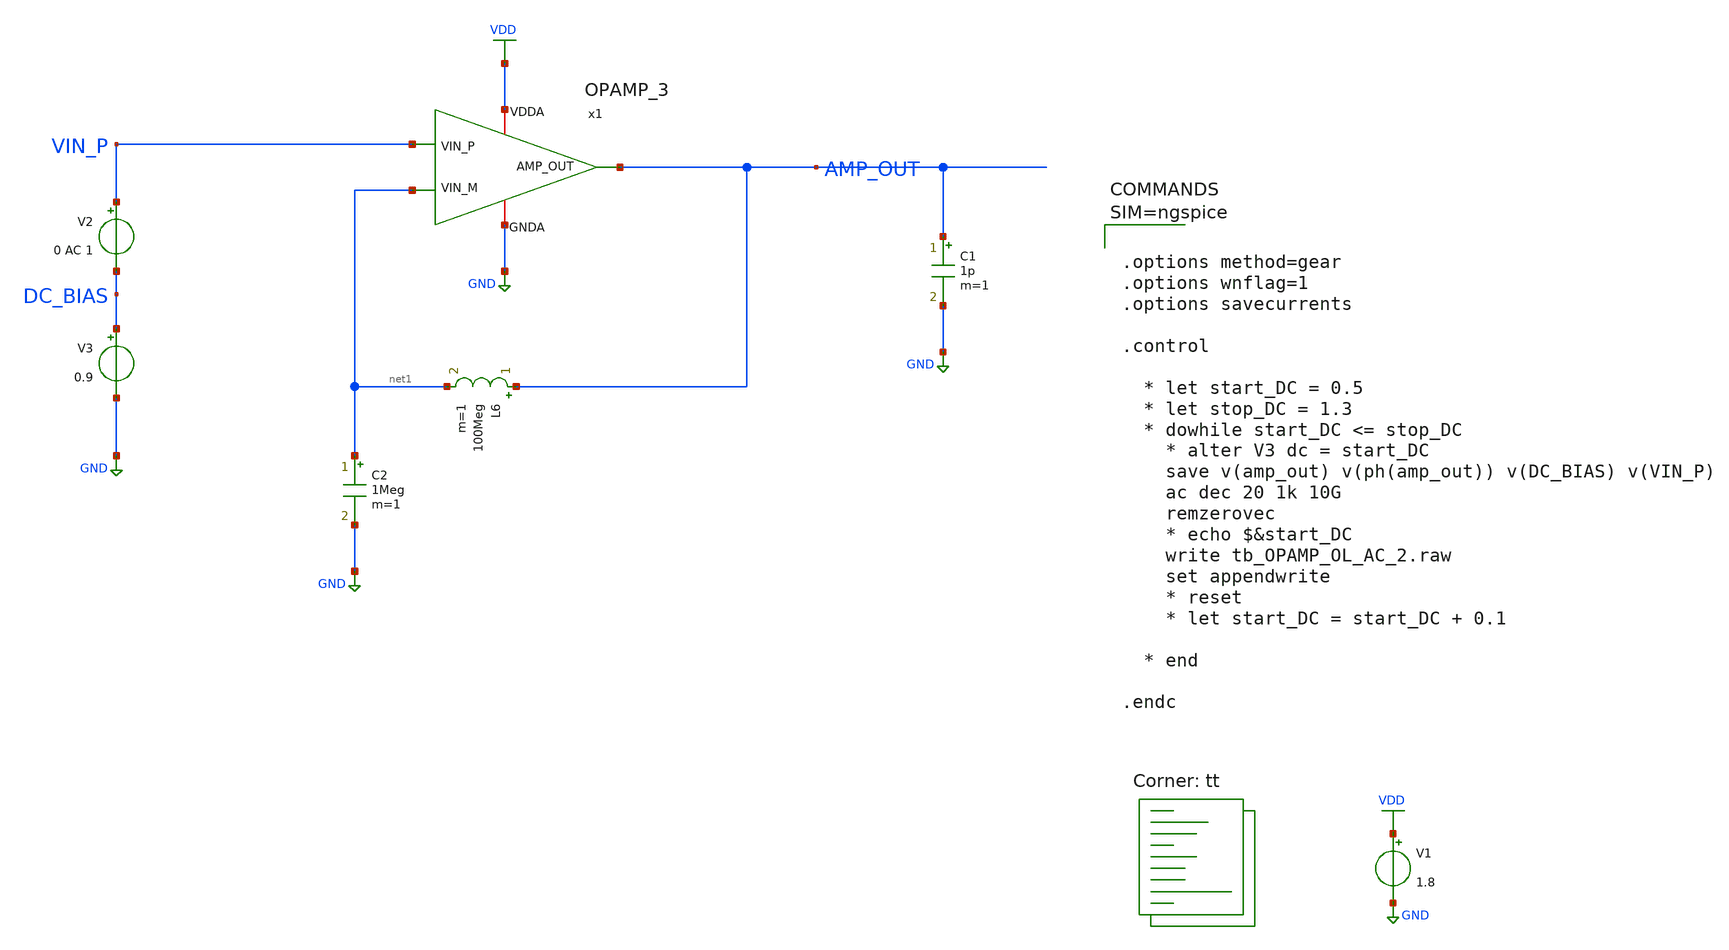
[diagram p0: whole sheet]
** sch_path: projects/ASU/EEE572/schematic/tb_OPAMP_OL_AC_2.sch
**.subckt tb_OPAMP_OL_AC_2
V1 VDD GND 1.8
V2 VIN_P DC_BIAS 0 AC 1
x1 VDD AMP_OUT VIN_P net1 GND OPAMP_3
V3 DC_BIAS GND 0.9
C1 AMP_OUT GND 1p m=1
C2 net1 GND 1Meg m=1
L6 AMP_OUT net1 100Meg m=1
**** begin user architecture code
.lib $::SKYWATER_MODELS/sky130.lib.spice tt



.options method=gear
.options wnflag=1
.options savecurrents

.control

  * let start_DC = 0.5
  * let stop_DC = 1.3
  * dowhile start_DC <= stop_DC
    * alter V3 dc = start_DC
    save v(amp_out) v(ph(amp_out)) v(DC_BIAS) v(VIN_P)
    ac dec 20 1k 10G
    remzerovec
    * echo $&start_DC
    write tb_OPAMP_OL_AC_2.raw
    set appendwrite
    * reset
    * let start_DC = start_DC + 0.1

  * end

.endc




**** end user architecture code
**.ends

* expanding   symbol:  OPAMP_3.sym # of pins=5
** sym_path: projects/ASU/EEE572/schematic/OPAMP_3.sym
** sch_path: projects/ASU/EEE572/schematic/OPAMP_3.sch
.subckt OPAMP_3 VDDA AMP_OUT VIN_P VIN_M GNDA
*.iopin GNDA
*.iopin VDDA
*.iopin VIN_M
*.iopin VIN_P
*.iopin AMP_OUT
XM1 V_REF V_REF V_RES GNDA sky130_fd_pr__nfet_01v8 L=0.3 W=16 nf=8 ad='int((nf+1)/2) * W/nf * 0.29' as='int((nf+2)/2) * W/nf * 0.29'
+ pd='2*int((nf+1)/2) * (W/nf + 0.29)' ps='2*int((nf+2)/2) * (W/nf + 0.29)' nrd='0.29 / W' nrs='0.29 / W'
+ sa=0 sb=0 sd=0 mult=1 m=1
XM2 V_REF_MIR V_REF_MIR GNDA GNDA sky130_fd_pr__nfet_01v8 L=0.3 W=4 nf=2 ad='int((nf+1)/2) * W/nf * 0.29'
+ as='int((nf+2)/2) * W/nf * 0.29' pd='2*int((nf+1)/2) * (W/nf + 0.29)' ps='2*int((nf+2)/2) * (W/nf + 0.29)'
+ nrd='0.29 / W' nrs='0.29 / W' sa=0 sb=0 sd=0 mult=1 m=1
XM5 START_UP V_REF_MIR GNDA GNDA sky130_fd_pr__nfet_01v8 L=0.3 W=4 nf=2 ad='int((nf+1)/2) * W/nf * 0.29'
+ as='int((nf+2)/2) * W/nf * 0.29' pd='2*int((nf+1)/2) * (W/nf + 0.29)' ps='2*int((nf+2)/2) * (W/nf + 0.29)'
+ nrd='0.29 / W' nrs='0.29 / W' sa=0 sb=0 sd=0 mult=1 m=1
XM7 Vbiasp START_UP V_REF_MIR GNDA sky130_fd_pr__nfet_01v8 L=0.3 W=4 nf=2 ad='int((nf+1)/2) * W/nf * 0.29'
+ as='int((nf+2)/2) * W/nf * 0.29' pd='2*int((nf+1)/2) * (W/nf + 0.29)' ps='2*int((nf+2)/2) * (W/nf + 0.29)'
+ nrd='0.29 / W' nrs='0.29 / W' sa=0 sb=0 sd=0 mult=1 m=1
XM6 START_UP START_UP VDD VDD sky130_fd_pr__pfet_01v8 L=20 W=0.5 nf=1 ad='int((nf+1)/2) * W/nf * 0.29'
+ as='int((nf+2)/2) * W/nf * 0.29' pd='2*int((nf+1)/2) * (W/nf + 0.29)' ps='2*int((nf+2)/2) * (W/nf + 0.29)'
+ nrd='0.29 / W' nrs='0.29 / W' sa=0 sb=0 sd=0 mult=1 m=1
XM3 V_REF Vbiasp VDDA VDDA sky130_fd_pr__pfet_01v8 L=0.3 W=12 nf=6 ad='int((nf+1)/2) * W/nf * 0.29' as='int((nf+2)/2) * W/nf * 0.29'
+ pd='2*int((nf+1)/2) * (W/nf + 0.29)' ps='2*int((nf+2)/2) * (W/nf + 0.29)' nrd='0.29 / W' nrs='0.29 / W'
+ sa=0 sb=0 sd=0 mult=1 m=1
XM4 V_REF_MIR Vbiasp VDDA VDDA sky130_fd_pr__pfet_01v8 L=0.3 W=12 nf=6 ad='int((nf+1)/2) * W/nf * 0.29'
+ as='int((nf+2)/2) * W/nf * 0.29' pd='2*int((nf+1)/2) * (W/nf + 0.29)' ps='2*int((nf+2)/2) * (W/nf + 0.29)'
+ nrd='0.29 / W' nrs='0.29 / W' sa=0 sb=0 sd=0 mult=1 m=1
XM8 Vbiasp V_REF_MIR GNDA GNDA sky130_fd_pr__nfet_01v8 L=0.3 W=4 nf=2 ad='int((nf+1)/2) * W/nf * 0.29'
+ as='int((nf+2)/2) * W/nf * 0.29' pd='2*int((nf+1)/2) * (W/nf + 0.29)' ps='2*int((nf+2)/2) * (W/nf + 0.29)'
+ nrd='0.29 / W' nrs='0.29 / W' sa=0 sb=0 sd=0 mult=1 m=1
XM9 Vbiasp_MIR V_REF GNDA GNDA sky130_fd_pr__nfet_01v8 L=0.3 W=4 nf=2 ad='int((nf+1)/2) * W/nf * 0.29'
+ as='int((nf+2)/2) * W/nf * 0.29' pd='2*int((nf+1)/2) * (W/nf + 0.29)' ps='2*int((nf+2)/2) * (W/nf + 0.29)'
+ nrd='0.29 / W' nrs='0.29 / W' sa=0 sb=0 sd=0 mult=1 m=1
XM10 Vbiasp Vbiasp_MIR VDDA VDDA sky130_fd_pr__pfet_01v8 L=0.3 W=12 nf=6 ad='int((nf+1)/2) * W/nf * 0.29'
+ as='int((nf+2)/2) * W/nf * 0.29' pd='2*int((nf+1)/2) * (W/nf + 0.29)' ps='2*int((nf+2)/2) * (W/nf + 0.29)'
+ nrd='0.29 / W' nrs='0.29 / W' sa=0 sb=0 sd=0 mult=1 m=1
XM11 Vbiasp_MIR Vbiasp_MIR VDDA VDDA sky130_fd_pr__pfet_01v8 L=0.3 W=12 nf=6 ad='int((nf+1)/2) * W/nf * 0.29'
+ as='int((nf+2)/2) * W/nf * 0.29' pd='2*int((nf+1)/2) * (W/nf + 0.29)' ps='2*int((nf+2)/2) * (W/nf + 0.29)'
+ nrd='0.29 / W' nrs='0.29 / W' sa=0 sb=0 sd=0 mult=1 m=1
XM12 Vbias3 Vbias3 GNDA GNDA sky130_fd_pr__nfet_01v8 L=4 W=4 nf=1 ad='int((nf+1)/2) * W/nf * 0.29' as='int((nf+2)/2) * W/nf * 0.29'
+ pd='2*int((nf+1)/2) * (W/nf + 0.29)' ps='2*int((nf+2)/2) * (W/nf + 0.29)' nrd='0.29 / W' nrs='0.29 / W'
+ sa=0 sb=0 sd=0 mult=1 m=1
XM13 Vbias3 Vbiasp VDDA VDDA sky130_fd_pr__pfet_01v8 L=0.3 W=12 nf=6 ad='int((nf+1)/2) * W/nf * 0.29'
+ as='int((nf+2)/2) * W/nf * 0.29' pd='2*int((nf+1)/2) * (W/nf + 0.29)' ps='2*int((nf+2)/2) * (W/nf + 0.29)'
+ nrd='0.29 / W' nrs='0.29 / W' sa=0 sb=0 sd=0 mult=1 m=1
XM14 net1 Vbias1 VDDA VDDA sky130_fd_pr__pfet_01v8 L=0.3 W=12 nf=6 ad='int((nf+1)/2) * W/nf * 0.29' as='int((nf+2)/2) * W/nf * 0.29'
+ pd='2*int((nf+1)/2) * (W/nf + 0.29)' ps='2*int((nf+2)/2) * (W/nf + 0.29)' nrd='0.29 / W' nrs='0.29 / W'
+ sa=0 sb=0 sd=0 mult=1 m=1
XM15 Vhigh Vbias1 VDDA VDDA sky130_fd_pr__pfet_01v8 L=0.3 W=12 nf=6 ad='int((nf+1)/2) * W/nf * 0.29'
+ as='int((nf+2)/2) * W/nf * 0.29' pd='2*int((nf+1)/2) * (W/nf + 0.29)' ps='2*int((nf+2)/2) * (W/nf + 0.29)'
+ nrd='0.29 / W' nrs='0.29 / W' sa=0 sb=0 sd=0 mult=1 m=1
XM16 Vncas Vbias2 net1 VDDA sky130_fd_pr__pfet_01v8 L=0.3 W=12 nf=6 ad='int((nf+1)/2) * W/nf * 0.29'
+ as='int((nf+2)/2) * W/nf * 0.29' pd='2*int((nf+1)/2) * (W/nf + 0.29)' ps='2*int((nf+2)/2) * (W/nf + 0.29)'
+ nrd='0.29 / W' nrs='0.29 / W' sa=0 sb=0 sd=0 mult=1 m=1
XM17 Vbias1 Vbias2 Vhigh VDDA sky130_fd_pr__pfet_01v8 L=0.3 W=12 nf=6 ad='int((nf+1)/2) * W/nf * 0.29'
+ as='int((nf+2)/2) * W/nf * 0.29' pd='2*int((nf+1)/2) * (W/nf + 0.29)' ps='2*int((nf+2)/2) * (W/nf + 0.29)'
+ nrd='0.29 / W' nrs='0.29 / W' sa=0 sb=0 sd=0 mult=1 m=1
XM18 net2 Vbias4 GNDA GNDA sky130_fd_pr__nfet_01v8 L=0.3 W=4 nf=2 ad='int((nf+1)/2) * W/nf * 0.29' as='int((nf+2)/2) * W/nf * 0.29'
+ pd='2*int((nf+1)/2) * (W/nf + 0.29)' ps='2*int((nf+2)/2) * (W/nf + 0.29)' nrd='0.29 / W' nrs='0.29 / W'
+ sa=0 sb=0 sd=0 mult=1 m=1
XM19 Vncas Vncas Vncas_btw GNDA sky130_fd_pr__nfet_01v8 L=0.3 W=4 nf=2 ad='int((nf+1)/2) * W/nf * 0.29'
+ as='int((nf+2)/2) * W/nf * 0.29' pd='2*int((nf+1)/2) * (W/nf + 0.29)' ps='2*int((nf+2)/2) * (W/nf + 0.29)'
+ nrd='0.29 / W' nrs='0.29 / W' sa=0 sb=0 sd=0 mult=1 m=1
XM20 Vncas_btw Vbias3 net3 GNDA sky130_fd_pr__nfet_01v8 L=0.3 W=4 nf=2 ad='int((nf+1)/2) * W/nf * 0.29'
+ as='int((nf+2)/2) * W/nf * 0.29' pd='2*int((nf+1)/2) * (W/nf + 0.29)' ps='2*int((nf+2)/2) * (W/nf + 0.29)'
+ nrd='0.29 / W' nrs='0.29 / W' sa=0 sb=0 sd=0 mult=1 m=1
XM21 net3 Vncas_btw GNDA GNDA sky130_fd_pr__nfet_01v8 L=0.3 W=4 nf=2 ad='int((nf+1)/2) * W/nf * 0.29'
+ as='int((nf+2)/2) * W/nf * 0.29' pd='2*int((nf+1)/2) * (W/nf + 0.29)' ps='2*int((nf+2)/2) * (W/nf + 0.29)'
+ nrd='0.29 / W' nrs='0.29 / W' sa=0 sb=0 sd=0 mult=1 m=1
XM25 Vbias4 Vbiasp VDDA VDDA sky130_fd_pr__pfet_01v8 L=0.3 W=12 nf=6 ad='int((nf+1)/2) * W/nf * 0.29'
+ as='int((nf+2)/2) * W/nf * 0.29' pd='2*int((nf+1)/2) * (W/nf + 0.29)' ps='2*int((nf+2)/2) * (W/nf + 0.29)'
+ nrd='0.29 / W' nrs='0.29 / W' sa=0 sb=0 sd=0 mult=1 m=1
XM27 Vbias4 Vbias3 Vlow GNDA sky130_fd_pr__nfet_01v8 L=0.3 W=4 nf=2 ad='int((nf+1)/2) * W/nf * 0.29'
+ as='int((nf+2)/2) * W/nf * 0.29' pd='2*int((nf+1)/2) * (W/nf + 0.29)' ps='2*int((nf+2)/2) * (W/nf + 0.29)'
+ nrd='0.29 / W' nrs='0.29 / W' sa=0 sb=0 sd=0 mult=1 m=1
XM28 Vlow Vbias4 GNDA GNDA sky130_fd_pr__nfet_01v8 L=0.3 W=4 nf=2 ad='int((nf+1)/2) * W/nf * 0.29' as='int((nf+2)/2) * W/nf * 0.29'
+ pd='2*int((nf+1)/2) * (W/nf + 0.29)' ps='2*int((nf+2)/2) * (W/nf + 0.29)' nrd='0.29 / W' nrs='0.29 / W'
+ sa=0 sb=0 sd=0 mult=1 m=1
XM29 Vds2 Vgs2 VDDA VDDA sky130_fd_pr__pfet_01v8 L=0.15 W=12 nf=6 ad='int((nf+1)/2) * W/nf * 0.29' as='int((nf+2)/2) * W/nf * 0.29'
+ pd='2*int((nf+1)/2) * (W/nf + 0.29)' ps='2*int((nf+2)/2) * (W/nf + 0.29)' nrd='0.29 / W' nrs='0.29 / W'
+ sa=0 sb=0 sd=0 mult=1 m=1
XM30 Vgs2 Vbias2 Vds2 VDDA sky130_fd_pr__pfet_01v8 L=0.15 W=12 nf=6 ad='int((nf+1)/2) * W/nf * 0.29'
+ as='int((nf+2)/2) * W/nf * 0.29' pd='2*int((nf+1)/2) * (W/nf + 0.29)' ps='2*int((nf+2)/2) * (W/nf + 0.29)'
+ nrd='0.29 / W' nrs='0.29 / W' sa=0 sb=0 sd=0 mult=1 m=1
XM31 Vpcas Vbias3 Vds3 GNDA sky130_fd_pr__nfet_01v8 L=0.3 W=4 nf=2 ad='int((nf+1)/2) * W/nf * 0.29' as='int((nf+2)/2) * W/nf * 0.29'
+ pd='2*int((nf+1)/2) * (W/nf + 0.29)' ps='2*int((nf+2)/2) * (W/nf + 0.29)' nrd='0.29 / W' nrs='0.29 / W'
+ sa=0 sb=0 sd=0 mult=1 m=1
XM32 Vds3 Vbias4 GNDA GNDA sky130_fd_pr__nfet_01v8 L=0.3 W=4 nf=2 ad='int((nf+1)/2) * W/nf * 0.29' as='int((nf+2)/2) * W/nf * 0.29'
+ pd='2*int((nf+1)/2) * (W/nf + 0.29)' ps='2*int((nf+2)/2) * (W/nf + 0.29)' nrd='0.29 / W' nrs='0.29 / W'
+ sa=0 sb=0 sd=0 mult=1 m=1
XM33 Vpcas Vpcas Vgs2 VDDA sky130_fd_pr__pfet_01v8 L=0.15 W=12 nf=1 ad='int((nf+1)/2) * W/nf * 0.29'
+ as='int((nf+2)/2) * W/nf * 0.29' pd='2*int((nf+1)/2) * (W/nf + 0.29)' ps='2*int((nf+2)/2) * (W/nf + 0.29)'
+ nrd='0.29 / W' nrs='0.29 / W' sa=0 sb=0 sd=0 mult=1 m=1
XM22 Vbias1 Vbias3 net2 GNDA sky130_fd_pr__nfet_01v8 L=0.3 W=4 nf=2 ad='int((nf+1)/2) * W/nf * 0.29'
+ as='int((nf+2)/2) * W/nf * 0.29' pd='2*int((nf+1)/2) * (W/nf + 0.29)' ps='2*int((nf+2)/2) * (W/nf + 0.29)'
+ nrd='0.29 / W' nrs='0.29 / W' sa=0 sb=0 sd=0 mult=1 m=1
XM23 Vbias2 Vbias2 VDDA VDDA sky130_fd_pr__pfet_01v8 L=1.5 W=12 nf=1 ad='int((nf+1)/2) * W/nf * 0.29'
+ as='int((nf+2)/2) * W/nf * 0.29' pd='2*int((nf+1)/2) * (W/nf + 0.29)' ps='2*int((nf+2)/2) * (W/nf + 0.29)'
+ nrd='0.29 / W' nrs='0.29 / W' sa=0 sb=0 sd=0 mult=1 m=1
XM24 net4 Vbias4 GNDA GNDA sky130_fd_pr__nfet_01v8 L=0.3 W=4 nf=2 ad='int((nf+1)/2) * W/nf * 0.29' as='int((nf+2)/2) * W/nf * 0.29'
+ pd='2*int((nf+1)/2) * (W/nf + 0.29)' ps='2*int((nf+2)/2) * (W/nf + 0.29)' nrd='0.29 / W' nrs='0.29 / W'
+ sa=0 sb=0 sd=0 mult=1 m=1
XM26 Vbias2 Vbias3 net4 GNDA sky130_fd_pr__nfet_01v8 L=0.3 W=4 nf=2 ad='int((nf+1)/2) * W/nf * 0.29'
+ as='int((nf+2)/2) * W/nf * 0.29' pd='2*int((nf+1)/2) * (W/nf + 0.29)' ps='2*int((nf+2)/2) * (W/nf + 0.29)'
+ nrd='0.29 / W' nrs='0.29 / W' sa=0 sb=0 sd=0 mult=1 m=1
XC1 Vbiasp VDDA sky130_fd_pr__cap_mim_m3_1 W=2 L=2 MF=4 m=4
XR1 GNDA V_RES GNDA sky130_fd_pr__res_high_po_0p35 L=0.5 mult=1 m=1
XM34 V_tail_btw Vbias4 GNDA GNDA sky130_fd_pr__nfet_01v8 L=0.3 W=12 nf=4 ad='int((nf+1)/2) * W/nf * 0.29'
+ as='int((nf+2)/2) * W/nf * 0.29' pd='2*int((nf+1)/2) * (W/nf + 0.29)' ps='2*int((nf+2)/2) * (W/nf + 0.29)'
+ nrd='0.29 / W' nrs='0.29 / W' sa=0 sb=0 sd=0 mult=3 m=3
XM35 Vp Vbias3 V_tail_btw GNDA sky130_fd_pr__nfet_01v8 L=0.3 W=12 nf=4 ad='int((nf+1)/2) * W/nf * 0.29'
+ as='int((nf+2)/2) * W/nf * 0.29' pd='2*int((nf+1)/2) * (W/nf + 0.29)' ps='2*int((nf+2)/2) * (W/nf + 0.29)'
+ nrd='0.29 / W' nrs='0.29 / W' sa=0 sb=0 sd=0 mult=3 m=3
XM36 Vd1 VIN_P Vp GNDA sky130_fd_pr__nfet_01v8 L=0.3 W=12 nf=1 ad='int((nf+1)/2) * W/nf * 0.29' as='int((nf+2)/2) * W/nf * 0.29'
+ pd='2*int((nf+1)/2) * (W/nf + 0.29)' ps='2*int((nf+2)/2) * (W/nf + 0.29)' nrd='0.29 / W' nrs='0.29 / W'
+ sa=0 sb=0 sd=0 mult=4 m=4
XM37 Vd2 VIN_M Vp GNDA sky130_fd_pr__nfet_01v8 L=0.3 W=12 nf=1 ad='int((nf+1)/2) * W/nf * 0.29' as='int((nf+2)/2) * W/nf * 0.29'
+ pd='2*int((nf+1)/2) * (W/nf + 0.29)' ps='2*int((nf+2)/2) * (W/nf + 0.29)' nrd='0.29 / W' nrs='0.29 / W'
+ sa=0 sb=0 sd=0 mult=4 m=4
XM38 AMP_MIR Vb1 Vd1 GNDA sky130_fd_pr__nfet_01v8 L=0.3 W=12 nf=1 ad='int((nf+1)/2) * W/nf * 0.29' as='int((nf+2)/2) * W/nf * 0.29'
+ pd='2*int((nf+1)/2) * (W/nf + 0.29)' ps='2*int((nf+2)/2) * (W/nf + 0.29)' nrd='0.29 / W' nrs='0.29 / W'
+ sa=0 sb=0 sd=0 mult=4 m=4
XM39 AMP_OUT Vb1 Vd2 GNDA sky130_fd_pr__nfet_01v8 L=0.3 W=12 nf=1 ad='int((nf+1)/2) * W/nf * 0.29' as='int((nf+2)/2) * W/nf * 0.29'
+ pd='2*int((nf+1)/2) * (W/nf + 0.29)' ps='2*int((nf+2)/2) * (W/nf + 0.29)' nrd='0.29 / W' nrs='0.29 / W'
+ sa=0 sb=0 sd=0 mult=4 m=4
XM40 net6 AMP_MIR VDDA VDDA sky130_fd_pr__pfet_01v8 L=0.3 W=12 nf=1 ad='int((nf+1)/2) * W/nf * 0.29'
+ as='int((nf+2)/2) * W/nf * 0.29' pd='2*int((nf+1)/2) * (W/nf + 0.29)' ps='2*int((nf+2)/2) * (W/nf + 0.29)'
+ nrd='0.29 / W' nrs='0.29 / W' sa=0 sb=0 sd=0 mult=12 m=12
XM41 net5 AMP_MIR VDDA VDDA sky130_fd_pr__pfet_01v8 L=0.3 W=12 nf=1 ad='int((nf+1)/2) * W/nf * 0.29'
+ as='int((nf+2)/2) * W/nf * 0.29' pd='2*int((nf+1)/2) * (W/nf + 0.29)' ps='2*int((nf+2)/2) * (W/nf + 0.29)'
+ nrd='0.29 / W' nrs='0.29 / W' sa=0 sb=0 sd=0 mult=12 m=12
XM42 AMP_OUT Vbias2 net6 VDDA sky130_fd_pr__pfet_01v8 L=0.3 W=12 nf=1 ad='int((nf+1)/2) * W/nf * 0.29'
+ as='int((nf+2)/2) * W/nf * 0.29' pd='2*int((nf+1)/2) * (W/nf + 0.29)' ps='2*int((nf+2)/2) * (W/nf + 0.29)'
+ nrd='0.29 / W' nrs='0.29 / W' sa=0 sb=0 sd=0 mult=12 m=12
XM43 AMP_MIR Vbias2 net5 VDDA sky130_fd_pr__pfet_01v8 L=0.3 W=12 nf=1 ad='int((nf+1)/2) * W/nf * 0.29'
+ as='int((nf+2)/2) * W/nf * 0.29' pd='2*int((nf+1)/2) * (W/nf + 0.29)' ps='2*int((nf+2)/2) * (W/nf + 0.29)'
+ nrd='0.29 / W' nrs='0.29 / W' sa=0 sb=0 sd=0 mult=12 m=12
XM44 Vb1 Vb1 Vp GNDA sky130_fd_pr__nfet_01v8 L=1 W=1 nf=1 ad='int((nf+1)/2) * W/nf * 0.29' as='int((nf+2)/2) * W/nf * 0.29'
+ pd='2*int((nf+1)/2) * (W/nf + 0.29)' ps='2*int((nf+2)/2) * (W/nf + 0.29)' nrd='0.29 / W' nrs='0.29 / W'
+ sa=0 sb=0 sd=0 mult=1 m=1
XM45 net7 Vbias1 VDDA VDDA sky130_fd_pr__pfet_01v8 L=0.3 W=12 nf=4 ad='int((nf+1)/2) * W/nf * 0.29' as='int((nf+2)/2) * W/nf * 0.29'
+ pd='2*int((nf+1)/2) * (W/nf + 0.29)' ps='2*int((nf+2)/2) * (W/nf + 0.29)' nrd='0.29 / W' nrs='0.29 / W'
+ sa=0 sb=0 sd=0 mult=1 m=1
XM46 Vb1 Vbias2 net7 VDDA sky130_fd_pr__pfet_01v8 L=0.3 W=12 nf=4 ad='int((nf+1)/2) * W/nf * 0.29' as='int((nf+2)/2) * W/nf * 0.29'
+ pd='2*int((nf+1)/2) * (W/nf + 0.29)' ps='2*int((nf+2)/2) * (W/nf + 0.29)' nrd='0.29 / W' nrs='0.29 / W'
+ sa=0 sb=0 sd=0 mult=1 m=1
.ends

.GLOBAL GND
.GLOBAL VDD
.end
